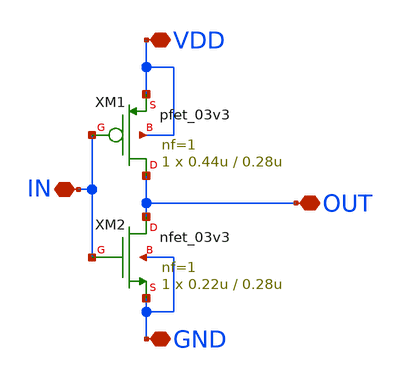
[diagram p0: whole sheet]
** sch_path: analog/design/inv/inv.sch
**.subckt inv OUT VDD GND IN
*.iopin OUT
*.iopin VDD
*.iopin GND
*.iopin IN
XM1 OUT IN VDD VDD pfet_03v3 L=0.28u W=0.44u nf=1 ad='int((nf+1)/2) * W/nf * 0.18u' as='int((nf+2)/2) * W/nf * 0.18u'
+ pd='2*int((nf+1)/2) * (W/nf + 0.18u)' ps='2*int((nf+2)/2) * (W/nf + 0.18u)' nrd='0.18u / W' nrs='0.18u / W'
+ sa=0 sb=0 sd=0 m=1
XM2 OUT IN GND GND nfet_03v3 L=0.28u W=0.22u nf=1 ad='int((nf+1)/2) * W/nf * 0.18u' as='int((nf+2)/2) * W/nf * 0.18u'
+ pd='2*int((nf+1)/2) * (W/nf + 0.18u)' ps='2*int((nf+2)/2) * (W/nf + 0.18u)' nrd='0.18u / W' nrs='0.18u / W'
+ sa=0 sb=0 sd=0 m=1
**.ends
.end
